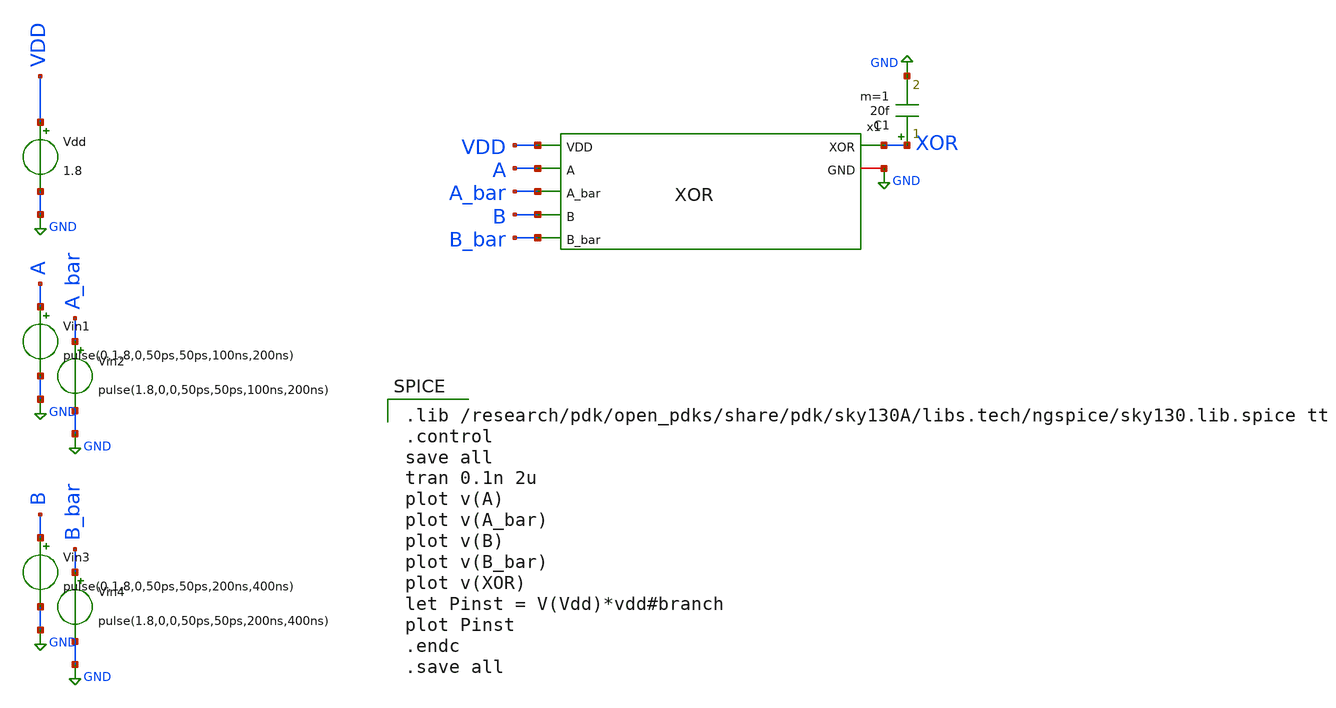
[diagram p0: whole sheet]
** sch_path: skywater_stuff/CMOS_XOR_sim.sch
**.subckt CMOS_XOR_sim
x1 A A_bar B B_bar XOR GND VDD XOR
Vdd VDD GND 1.8
Vin1 A GND pulse(0,1.8,0,50ps,50ps,100ns,200ns)
Vin2 A_bar GND pulse(1.8,0,0,50ps,50ps,100ns,200ns)
Vin3 B GND pulse(0,1.8,0,50ps,50ps,200ns,400ns)
Vin4 B_bar GND pulse(1.8,0,0,50ps,50ps,200ns,400ns)
C1 XOR GND 20f m=1
**** begin user architecture code

.lib /research/pdk/open_pdks/share/pdk/sky130A/libs.tech/ngspice/sky130.lib.spice tt
.control
save all
tran 0.1n 2u
plot v(A)
plot v(A_bar)
plot v(B)
plot v(B_bar)
plot v(XOR)
let Pinst = V(Vdd)*vdd#branch
plot Pinst
.endc
.save all

**** end user architecture code
**.ends

* expanding   symbol:  XOR.sym # of pins=7
** sym_path: skywater_stuff/XOR.sym
** sch_path: skywater_stuff/XOR.sch
.subckt XOR A A_bar B B_bar XOR GND VDD
*.ipin A
*.ipin A_bar
*.ipin B
*.ipin B_bar
*.opin XOR
*.iopin GND
*.ipin VDD
XM8 net4 A_bar GND GND sky130_fd_pr__nfet_01v8 L=0.15 W=1 nf=1 ad='int((nf+1)/2) * W/nf * 0.29' as='int((nf+2)/2) * W/nf * 0.29'
+ pd='2*int((nf+1)/2) * (W/nf + 0.29)' ps='2*int((nf+2)/2) * (W/nf + 0.29)' nrd='0.29 / W' nrs='0.29 / W'
+ sa=0 sb=0 sd=0 mult=1 m=1
XM1 XOR B net3 GND sky130_fd_pr__nfet_01v8 L=0.15 W=1 nf=1 ad='int((nf+1)/2) * W/nf * 0.29' as='int((nf+2)/2) * W/nf * 0.29'
+ pd='2*int((nf+1)/2) * (W/nf + 0.29)' ps='2*int((nf+2)/2) * (W/nf + 0.29)' nrd='0.29 / W' nrs='0.29 / W'
+ sa=0 sb=0 sd=0 mult=1 m=1
XM3 XOR A net1 VDD sky130_fd_pr__pfet_01v8 L=0.15 W=2 nf=1 ad='int((nf+1)/2) * W/nf * 0.29' as='int((nf+2)/2) * W/nf * 0.29'
+ pd='2*int((nf+1)/2) * (W/nf + 0.29)' ps='2*int((nf+2)/2) * (W/nf + 0.29)' nrd='0.29 / W' nrs='0.29 / W'
+ sa=0 sb=0 sd=0 mult=1 m=1
XM4 net2 B VDD VDD sky130_fd_pr__pfet_01v8 L=0.15 W=2 nf=1 ad='int((nf+1)/2) * W/nf * 0.29' as='int((nf+2)/2) * W/nf * 0.29'
+ pd='2*int((nf+1)/2) * (W/nf + 0.29)' ps='2*int((nf+2)/2) * (W/nf + 0.29)' nrd='0.29 / W' nrs='0.29 / W'
+ sa=0 sb=0 sd=0 mult=1 m=1
XM2 net1 B_bar VDD VDD sky130_fd_pr__pfet_01v8 L=0.15 W=2 nf=1 ad='int((nf+1)/2) * W/nf * 0.29' as='int((nf+2)/2) * W/nf * 0.29'
+ pd='2*int((nf+1)/2) * (W/nf + 0.29)' ps='2*int((nf+2)/2) * (W/nf + 0.29)' nrd='0.29 / W' nrs='0.29 / W'
+ sa=0 sb=0 sd=0 mult=1 m=1
XM7 XOR B_bar net4 GND sky130_fd_pr__nfet_01v8 L=0.15 W=1 nf=1 ad='int((nf+1)/2) * W/nf * 0.29' as='int((nf+2)/2) * W/nf * 0.29'
+ pd='2*int((nf+1)/2) * (W/nf + 0.29)' ps='2*int((nf+2)/2) * (W/nf + 0.29)' nrd='0.29 / W' nrs='0.29 / W'
+ sa=0 sb=0 sd=0 mult=1 m=1
XM6 net3 A GND GND sky130_fd_pr__nfet_01v8 L=0.15 W=1 nf=1 ad='int((nf+1)/2) * W/nf * 0.29' as='int((nf+2)/2) * W/nf * 0.29'
+ pd='2*int((nf+1)/2) * (W/nf + 0.29)' ps='2*int((nf+2)/2) * (W/nf + 0.29)' nrd='0.29 / W' nrs='0.29 / W'
+ sa=0 sb=0 sd=0 mult=1 m=1
XM5 XOR A_bar net2 VDD sky130_fd_pr__pfet_01v8 L=0.15 W=2 nf=1 ad='int((nf+1)/2) * W/nf * 0.29' as='int((nf+2)/2) * W/nf * 0.29'
+ pd='2*int((nf+1)/2) * (W/nf + 0.29)' ps='2*int((nf+2)/2) * (W/nf + 0.29)' nrd='0.29 / W' nrs='0.29 / W'
+ sa=0 sb=0 sd=0 mult=1 m=1
.ends

.GLOBAL GND
.end
